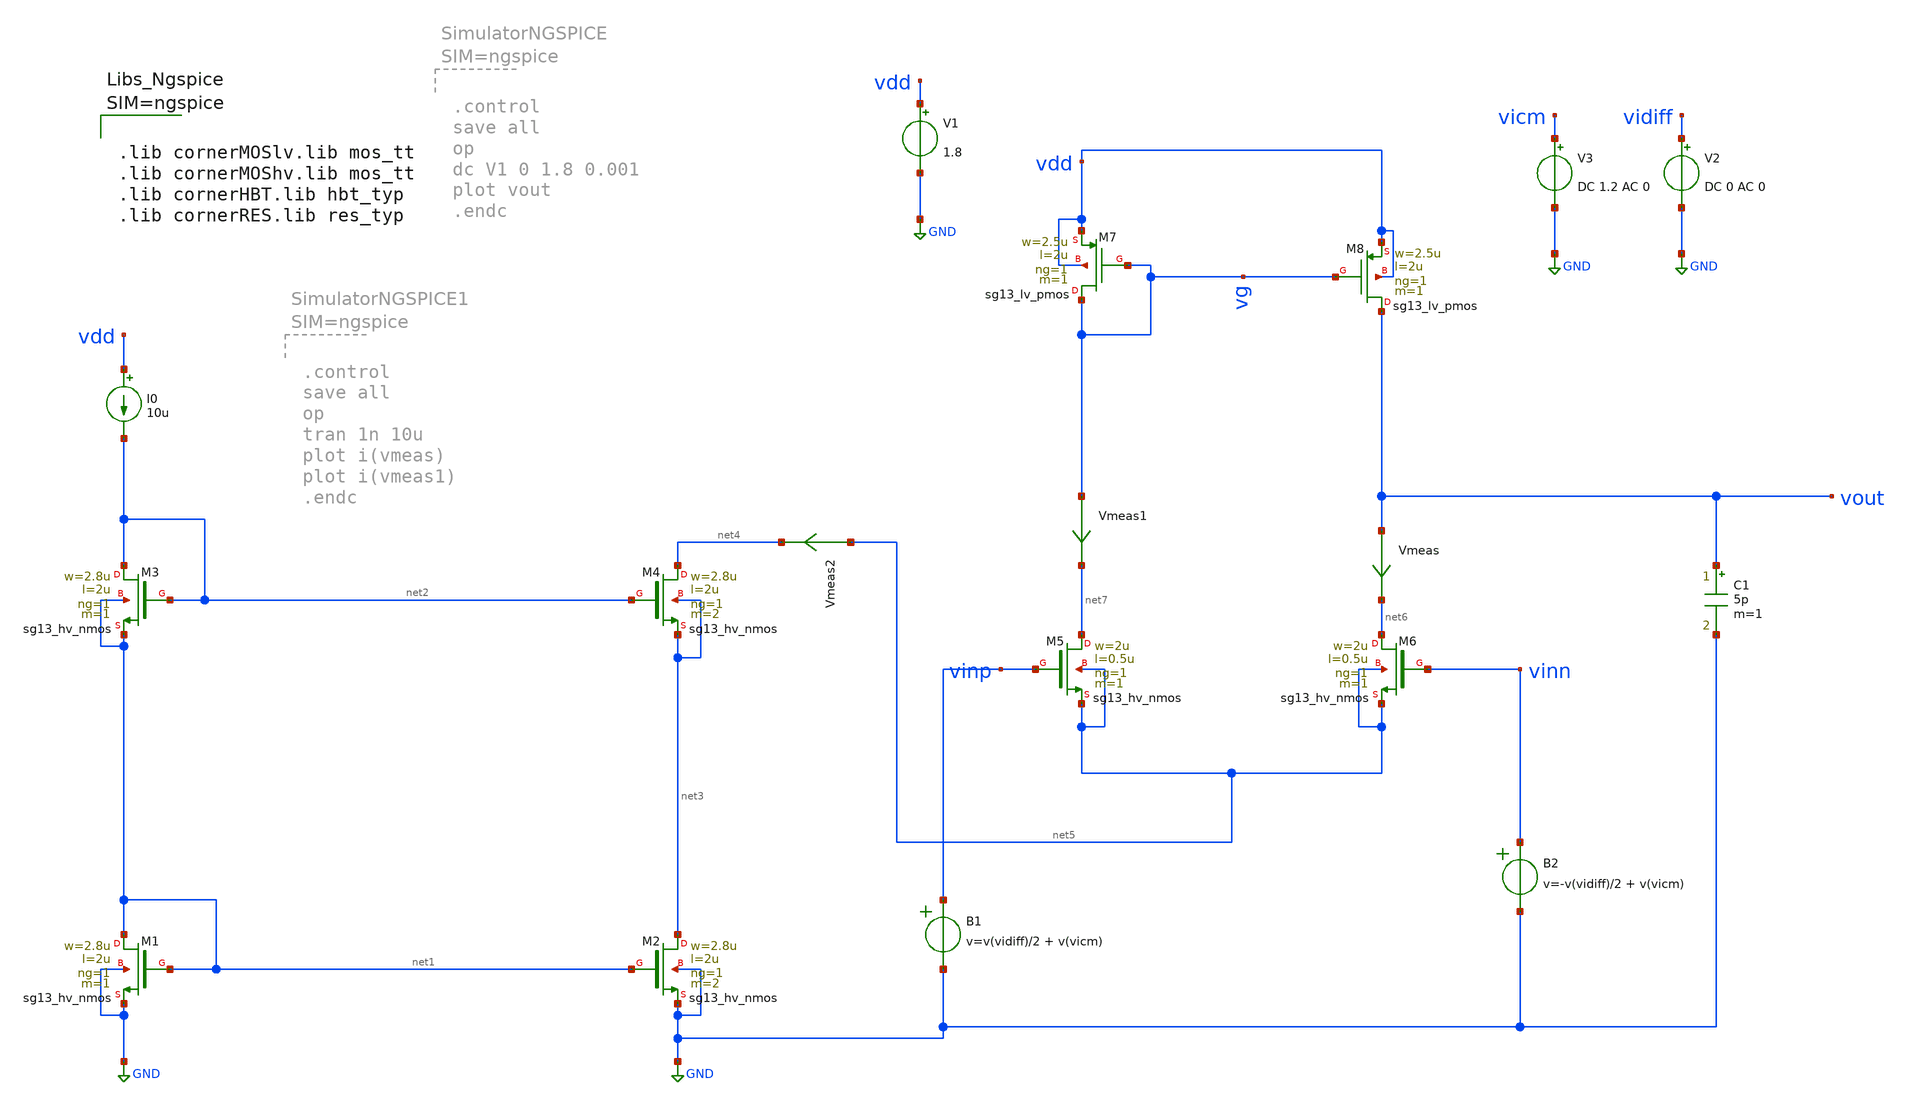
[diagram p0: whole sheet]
** sch_path: Schematics/5T_OTA.sch
**.subckt 5T_OTA
V1 vdd GND 1.8
I0 vdd net2 10u
XM1 net1 net1 GND GND sg13_hv_nmos w=2.8u l=2u ng=1 m=1 mm_ok=1
XM2 net3 net1 GND GND sg13_hv_nmos w=2.8u l=2u ng=1 m=2 mm_ok=1
XM3 net2 net2 net1 net1 sg13_hv_nmos w=2.8u l=2u ng=1 m=1 mm_ok=1
XM4 net4 net2 net3 net3 sg13_hv_nmos w=2.8u l=2u ng=1 m=2 mm_ok=1
XM5 net7 vinp net5 net5 sg13_hv_nmos w=2u l=0.5u ng=1 m=1 mm_ok=1
XM6 net6 vinn net5 net5 sg13_hv_nmos w=2u l=0.5u ng=1 m=1 mm_ok=1
V3 vicm GND DC 1.2 AC 0
Vmeas vout net6 0
.save i(vmeas)
Vmeas1 vg net7 0
.save i(vmeas1)
XM7 vg vg vdd vdd sg13_lv_pmos w=2.5u l=2u ng=1 m=1 mm_ok=1
XM8 vout vg vdd vdd sg13_lv_pmos w=2.5u l=2u ng=1 m=1 mm_ok=1
Vmeas2 net5 net4 0
.save i(vmeas2)
V2 vidiff GND DC 0 AC 0
B1 vinp GND v=v(vidiff)/2 + v(vicm)
B2 vinn GND v=-v(vidiff)/2 + v(vicm)
C1 vout GND 5p m=1
**** begin user architecture code



.lib cornerMOSlv.lib mos_tt
.lib cornerMOShv.lib mos_tt
.lib cornerHBT.lib hbt_typ
.lib cornerRES.lib res_typ



**** end user architecture code
**.ends
.GLOBAL GND
.end
